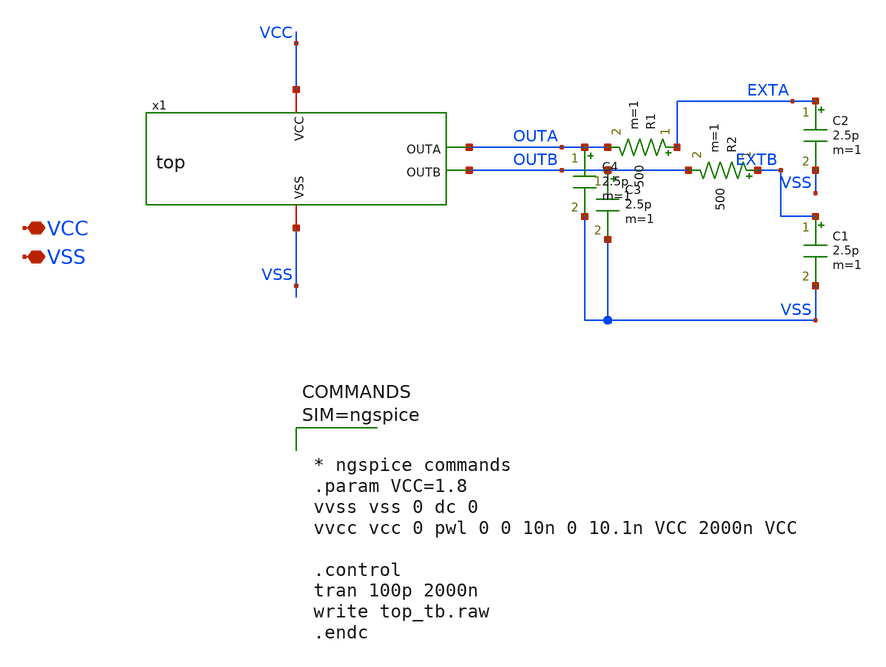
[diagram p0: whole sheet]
** sch_path: xschem/top_tb.sch
**.subckt top_tb VCC VSS
*.iopin VCC
*.iopin VSS
x1 VCC OUTA OUTB VSS top
R1 EXTA OUTA 500 m=1
R2 EXTB OUTB 500 m=1
C1 EXTB VSS 2.5p m=1
C2 EXTA VSS 2.5p m=1
C3 OUTB VSS 2.5p m=1
C4 OUTA VSS 2.5p m=1
**** begin user architecture code

** opencircuitdesign pdks install
.lib $::SKYWATER_MODELS/sky130.lib.spice tt





* ngspice commands
.param VCC=1.8
vvss vss 0 dc 0
vvcc vcc 0 pwl 0 0 10n 0 10.1n VCC 2000n VCC

.control
tran 100p 2000n
write top_tb.raw
.endc




**** end user architecture code
**.ends

* expanding   symbol:  top.sym # of pins=4
** sym_path: xschem/top.sym
** sch_path: xschem/top.sch
.subckt top VCC OUTA OUTB VSS
*.iopin VCC
*.iopin VSS
*.opin OUTA
*.opin OUTB
x1 VCC OUTA VSS oscillator_20MHZ
x2 VCC OUTB VSS oscillator_21MHZ
.ends


* expanding   symbol:  oscillator_20MHZ.sym # of pins=3
** sym_path: xschem/oscillator_20MHZ.sym
** sch_path: xschem/oscillator_20MHZ.sch
.subckt oscillator_20MHZ VCC OUT VSS
*.iopin VCC
*.iopin VSS
*.opin OUT
x1[30] INI[29] OUT_INI VCC VSS inverter
x1[29] INI[28] INI[29] VCC VSS inverter
x1[28] INI[27] INI[28] VCC VSS inverter
x1[27] INI[26] INI[27] VCC VSS inverter
x1[26] INI[25] INI[26] VCC VSS inverter
x1[25] INI[24] INI[25] VCC VSS inverter
x1[24] INI[23] INI[24] VCC VSS inverter
x1[23] INI[22] INI[23] VCC VSS inverter
x1[22] INI[21] INI[22] VCC VSS inverter
x1[21] INI[20] INI[21] VCC VSS inverter
x1[20] INI[19] INI[20] VCC VSS inverter
x1[19] INI[18] INI[19] VCC VSS inverter
x1[18] INI[17] INI[18] VCC VSS inverter
x1[17] INI[16] INI[17] VCC VSS inverter
x1[16] INI[15] INI[16] VCC VSS inverter
x1[15] INI[14] INI[15] VCC VSS inverter
x1[14] INI[13] INI[14] VCC VSS inverter
x1[13] INI[12] INI[13] VCC VSS inverter
x1[12] INI[11] INI[12] VCC VSS inverter
x1[11] INI[10] INI[11] VCC VSS inverter
x1[10] INI[9] INI[10] VCC VSS inverter
x1[9] INI[8] INI[9] VCC VSS inverter
x1[8] INI[7] INI[8] VCC VSS inverter
x1[7] INI[6] INI[7] VCC VSS inverter
x1[6] INI[5] INI[6] VCC VSS inverter
x1[5] INI[4] INI[5] VCC VSS inverter
x1[4] INI[3] INI[4] VCC VSS inverter
x1[3] INI[2] INI[3] VCC VSS inverter
x1[2] INI[1] INI[2] VCC VSS inverter
x1[1] INI[0] INI[1] VCC VSS inverter
x1[0] OUT_INI INI[0] VCC VSS inverter
x3 OUT OUT_INI VCC VSS inverter
.ends


* expanding   symbol:  oscillator_21MHZ.sym # of pins=3
** sym_path: xschem/oscillator_21MHZ.sym
** sch_path: xschem/oscillator_21MHZ.sch
.subckt oscillator_21MHZ VCC OUT VSS
*.iopin VCC
*.iopin VSS
*.opin OUT
x1[20] INI[19] OUT_INI VCC VSS inverter
x1[19] INI[18] INI[19] VCC VSS inverter
x1[18] INI[17] INI[18] VCC VSS inverter
x1[17] INI[16] INI[17] VCC VSS inverter
x1[16] INI[15] INI[16] VCC VSS inverter
x1[15] INI[14] INI[15] VCC VSS inverter
x1[14] INI[13] INI[14] VCC VSS inverter
x1[13] INI[12] INI[13] VCC VSS inverter
x1[12] INI[11] INI[12] VCC VSS inverter
x1[11] INI[10] INI[11] VCC VSS inverter
x1[10] INI[9] INI[10] VCC VSS inverter
x1[9] INI[8] INI[9] VCC VSS inverter
x1[8] INI[7] INI[8] VCC VSS inverter
x1[7] INI[6] INI[7] VCC VSS inverter
x1[6] INI[5] INI[6] VCC VSS inverter
x1[5] INI[4] INI[5] VCC VSS inverter
x1[4] INI[3] INI[4] VCC VSS inverter
x1[3] INI[2] INI[3] VCC VSS inverter
x1[2] INI[1] INI[2] VCC VSS inverter
x1[1] INI[0] INI[1] VCC VSS inverter
x1[0] OUT_INI INI[0] VCC VSS inverter
x1 OUT OUT_INI VCC VSS inverter
.ends


* expanding   symbol:  inverter.sym # of pins=4
** sym_path: xschem/inverter.sym
** sch_path: xschem/inverter.sch
.subckt inverter OUT IN VCC VSS
*.iopin VCC
*.iopin VSS
*.ipin IN
*.opin OUT
XM1 OUT IN net1 VCC sky130_fd_pr__pfet_01v8 L=1 W=2 nf=1 ad='int((nf+1)/2) * W/nf * 0.29' as='int((nf+2)/2) * W/nf * 0.29'
+ pd='2*int((nf+1)/2) * (W/nf + 0.29)' ps='2*int((nf+2)/2) * (W/nf + 0.29)' nrd='0.29 / W' nrs='0.29 / W'
+ sa=0 sb=0 sd=0 mult=1 m=1
XM2 OUT IN net2 VSS sky130_fd_pr__nfet_01v8 L=1 W=1 nf=1 ad='int((nf+1)/2) * W/nf * 0.29' as='int((nf+2)/2) * W/nf * 0.29'
+ pd='2*int((nf+1)/2) * (W/nf + 0.29)' ps='2*int((nf+2)/2) * (W/nf + 0.29)' nrd='0.29 / W' nrs='0.29 / W'
+ sa=0 sb=0 sd=0 mult=1 m=1
XM3 net1 VSS VCC VCC sky130_fd_pr__pfet_01v8 L=1 W=2 nf=1 ad='int((nf+1)/2) * W/nf * 0.29' as='int((nf+2)/2) * W/nf * 0.29'
+ pd='2*int((nf+1)/2) * (W/nf + 0.29)' ps='2*int((nf+2)/2) * (W/nf + 0.29)' nrd='0.29 / W' nrs='0.29 / W'
+ sa=0 sb=0 sd=0 mult=1 m=1
XM4 net2 VCC VSS VSS sky130_fd_pr__nfet_01v8 L=1 W=1 nf=1 ad='int((nf+1)/2) * W/nf * 0.29' as='int((nf+2)/2) * W/nf * 0.29'
+ pd='2*int((nf+1)/2) * (W/nf + 0.29)' ps='2*int((nf+2)/2) * (W/nf + 0.29)' nrd='0.29 / W' nrs='0.29 / W'
+ sa=0 sb=0 sd=0 mult=1 m=1
.ends

.end
